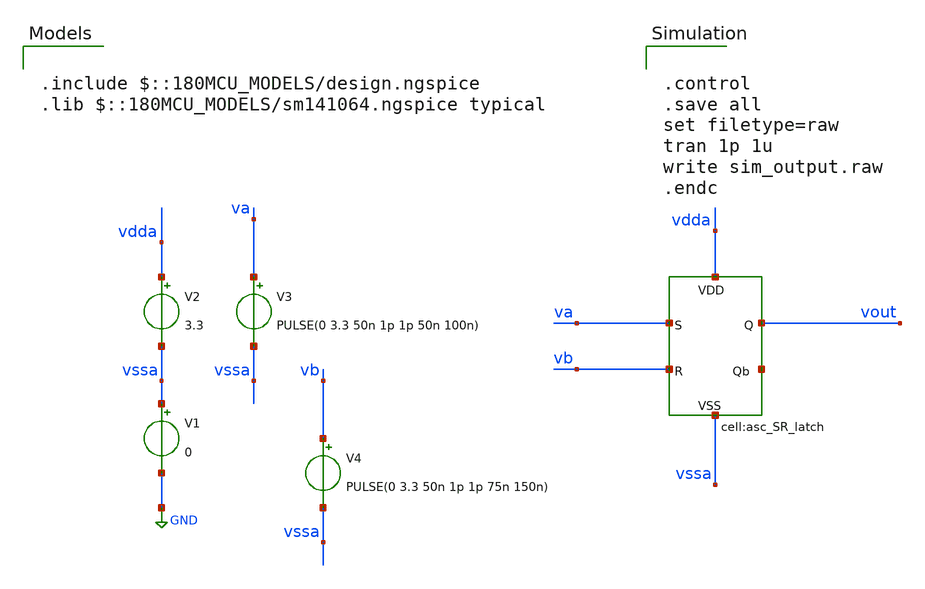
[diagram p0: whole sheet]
** sch_path: designs/libs/xp_tb_analog/tb_asc_SR_latch/tb_asc_SR_latch.sch
**.subckt tb_asc_SR_latch
V1 vssa GND 0
V2 vdda vssa 3.3
V3 va vssa PULSE(0 3.3 50n 1p 1p 50n 100n)
V4 vb vssa PULSE(0 3.3 50n 1p 1p 75n 150n)
x1 vb va net1 vdda vssa vout asc_SR_latch
**** begin user architecture code

.include $::180MCU_MODELS/design.ngspice
.lib $::180MCU_MODELS/sm141064.ngspice typical



.control
.save all
set filetype=raw
tran 1p 1u
write sim_output.raw
.endc


**** end user architecture code
**.ends

* expanding   symbol:  libs/core_analog/asc_SR_latch/asc_SR_latch.sym # of pins=6
** sym_path: designs/libs/xp_core_analog/asc_SR_latch/asc_SR_latch.sym
** sch_path: designs/libs/xp_core_analog/asc_SR_latch/asc_SR_latch.sch
.subckt asc_SR_latch R S Qb VDD VSS Q
*.iopin VDD
*.iopin VSS
*.iopin S
*.iopin R
*.iopin Qb
*.iopin Q
x1 VDD VSS Q R Qb asc_NOR
x2 VDD VSS Qb Q S asc_NOR
.ends


* expanding   symbol:  libs/core_analog/asc_NOR/asc_NOR.sym # of pins=5
** sym_path: designs/libs/xp_core_analog/asc_NOR/asc_NOR.sym
** sch_path: designs/libs/xp_core_analog/asc_NOR/asc_NOR.sch
.subckt asc_NOR VDD VSS OUT A B
*.iopin VDD
*.iopin VSS
*.iopin B
*.iopin A
*.iopin OUT
XM1 OUT A VSS VSS nfet_03v3 L=0.5u W=1u nf=1 ad='int((nf+1)/2) * W/nf * 0.18u' as='int((nf+2)/2) * W/nf * 0.18u'
+ pd='2*int((nf+1)/2) * (W/nf + 0.18u)' ps='2*int((nf+2)/2) * (W/nf + 0.18u)' nrd='0.18u / W' nrs='0.18u / W'
+ sa=0 sb=0 sd=0 m=1
XM2 OUT B VSS VSS nfet_03v3 L=0.5u W=1u nf=1 ad='int((nf+1)/2) * W/nf * 0.18u' as='int((nf+2)/2) * W/nf * 0.18u'
+ pd='2*int((nf+1)/2) * (W/nf + 0.18u)' ps='2*int((nf+2)/2) * (W/nf + 0.18u)' nrd='0.18u / W' nrs='0.18u / W'
+ sa=0 sb=0 sd=0 m=1
XM3 OUT B net1 VDD pfet_03v3 L=0.5u W=1u nf=6 ad='int((nf+1)/2) * W/nf * 0.18u' as='int((nf+2)/2) * W/nf * 0.18u'
+ pd='2*int((nf+1)/2) * (W/nf + 0.18u)' ps='2*int((nf+2)/2) * (W/nf + 0.18u)' nrd='0.18u / W' nrs='0.18u / W'
+ sa=0 sb=0 sd=0 m=1
XM4 net1 A VDD VDD pfet_03v3 L=0.5u W=1u nf=6 ad='int((nf+1)/2) * W/nf * 0.18u' as='int((nf+2)/2) * W/nf * 0.18u'
+ pd='2*int((nf+1)/2) * (W/nf + 0.18u)' ps='2*int((nf+2)/2) * (W/nf + 0.18u)' nrd='0.18u / W' nrs='0.18u / W'
+ sa=0 sb=0 sd=0 m=1
.ends

.GLOBAL GND
.end
